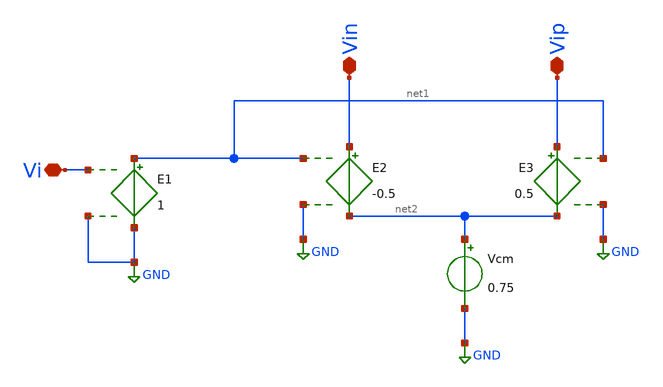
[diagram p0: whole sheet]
** sch_path: single_to_diff.sch
**.subckt single_to_diff Vi Vip Vin
*.iopin Vi
*.iopin Vip
*.iopin Vin
E1 net1 GND Vi GND 1
E2 Vin net2 net1 GND -0.5
E3 Vip net2 net1 GND 0.5
Vcm net2 GND 0.75
**.ends
.GLOBAL GND
.end
